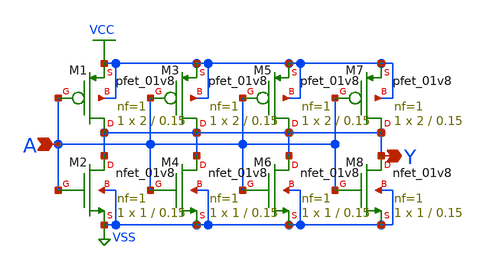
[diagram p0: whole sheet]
** sch_path: elements/logic/not_4.sch
**.subckt not_4 A Y
*.ipin A
*.opin Y
XM1 Y A VCC VCC sky130_fd_pr__pfet_01v8 L=0.15 W=2 nf=1 ad='int((nf+1)/2) * W/nf * 0.29' as='int((nf+2)/2) * W/nf * 0.29'
+ pd='2*int((nf+1)/2) * (W/nf + 0.29)' ps='2*int((nf+2)/2) * (W/nf + 0.29)' nrd='0.29 / W' nrs='0.29 / W'
+ sa=0 sb=0 sd=0 mult=1 m=1
XM2 Y A VSS VSS sky130_fd_pr__nfet_01v8 L=0.15 W=1 nf=1 ad='int((1 + 1)/2) * 1 / 1 * 0.29' as='int((1 + 2)/2) * 1 / 1 * 0.29'
+ pd='2*int((1 + 1)/2) * (1 / 1 + 0.29)' ps='2*int((1 + 2)/2) * (1 / 1 + 0.29)' nrd='0.29 / 1 ' nrs='0.29 / 1 '
+ sa=0 sb=0 sd=0 mult=1 m=1
XM3 Y A VCC VCC sky130_fd_pr__pfet_01v8 L=0.15 W=2 nf=1 ad='int((nf+1)/2) * W/nf * 0.29' as='int((nf+2)/2) * W/nf * 0.29'
+ pd='2*int((nf+1)/2) * (W/nf + 0.29)' ps='2*int((nf+2)/2) * (W/nf + 0.29)' nrd='0.29 / W' nrs='0.29 / W'
+ sa=0 sb=0 sd=0 mult=1 m=1
XM4 Y A VSS VSS sky130_fd_pr__nfet_01v8 L=0.15 W=1 nf=1 ad='int((1 + 1)/2) * 1 / 1 * 0.29' as='int((1 + 2)/2) * 1 / 1 * 0.29'
+ pd='2*int((1 + 1)/2) * (1 / 1 + 0.29)' ps='2*int((1 + 2)/2) * (1 / 1 + 0.29)' nrd='0.29 / 1 ' nrs='0.29 / 1 '
+ sa=0 sb=0 sd=0 mult=1 m=1
XM5 Y A VCC VCC sky130_fd_pr__pfet_01v8 L=0.15 W=2 nf=1 ad='int((nf+1)/2) * W/nf * 0.29' as='int((nf+2)/2) * W/nf * 0.29'
+ pd='2*int((nf+1)/2) * (W/nf + 0.29)' ps='2*int((nf+2)/2) * (W/nf + 0.29)' nrd='0.29 / W' nrs='0.29 / W'
+ sa=0 sb=0 sd=0 mult=1 m=1
XM6 Y A VSS VSS sky130_fd_pr__nfet_01v8 L=0.15 W=1 nf=1 ad='int((1 + 1)/2) * 1 / 1 * 0.29' as='int((1 + 2)/2) * 1 / 1 * 0.29'
+ pd='2*int((1 + 1)/2) * (1 / 1 + 0.29)' ps='2*int((1 + 2)/2) * (1 / 1 + 0.29)' nrd='0.29 / 1 ' nrs='0.29 / 1 '
+ sa=0 sb=0 sd=0 mult=1 m=1
XM7 Y A VCC VCC sky130_fd_pr__pfet_01v8 L=0.15 W=2 nf=1 ad='int((nf+1)/2) * W/nf * 0.29' as='int((nf+2)/2) * W/nf * 0.29'
+ pd='2*int((nf+1)/2) * (W/nf + 0.29)' ps='2*int((nf+2)/2) * (W/nf + 0.29)' nrd='0.29 / W' nrs='0.29 / W'
+ sa=0 sb=0 sd=0 mult=1 m=1
XM8 Y A VSS VSS sky130_fd_pr__nfet_01v8 L=0.15 W=1 nf=1 ad='int((1 + 1)/2) * 1 / 1 * 0.29' as='int((1 + 2)/2) * 1 / 1 * 0.29'
+ pd='2*int((1 + 1)/2) * (1 / 1 + 0.29)' ps='2*int((1 + 2)/2) * (1 / 1 + 0.29)' nrd='0.29 / 1 ' nrs='0.29 / 1 '
+ sa=0 sb=0 sd=0 mult=1 m=1
**.ends
.GLOBAL VCC
.GLOBAL VSS
.end
